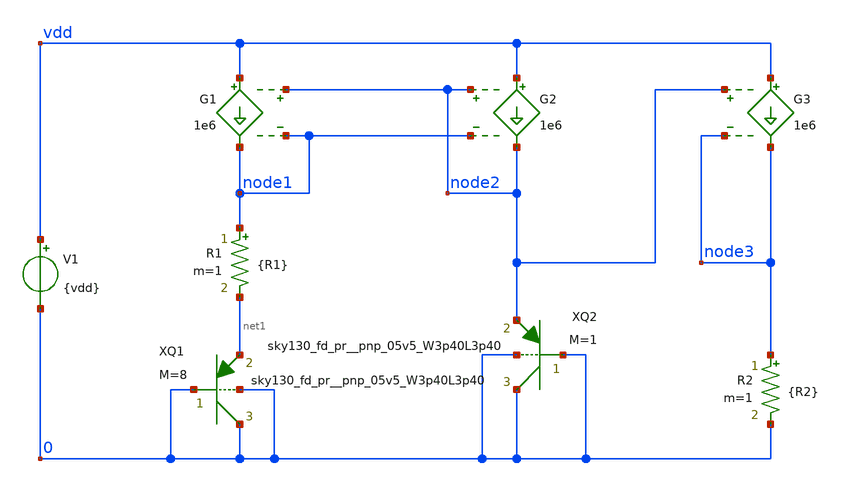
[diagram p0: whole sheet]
** sch_path: xschem/bandgap_core_mod/test/archive/ideal_bandgap_test.sch
**.subckt ideal_bandgap_test
R1 node1 net1 {R1} m=1
R2 node3 0 {R2} m=1
XQ1 0 0 net1 0 sky130_fd_pr__pnp_05v5_W3p40L3p40 m=8
XQ2 0 0 node2 0 sky130_fd_pr__pnp_05v5_W3p40L3p40 m=1
G1 vdd node1 node2 node1 1e6
G2 vdd node2 node2 node1 1e6
G3 vdd node3 node2 node3 1e6
V1 vdd 0 {vdd}
**** begin user architecture code


.temp 27

.lib sky130_fd_pr/models/sky130.lib.spice tt
.include sky130_fd_pr/models/sky130_fd_pr__model__pnp.model.spice

.param vdd=1.8
.param R1=10k
.param R2=10k

.options savecurrents

.dc temp -40 125 1.65

** add an extra startup current source
Gsu vdd node2 cur='500*max(0,(0.5-v(node2)))'


**** end user architecture code
**.ends
.end
